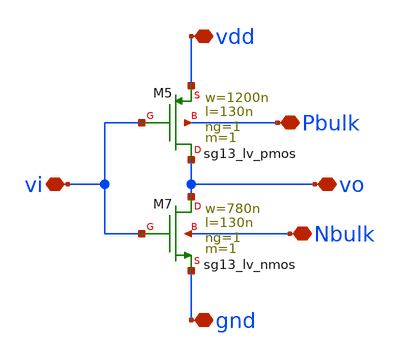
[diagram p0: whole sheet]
** sch_path: dependencies/SAH/SAH-main/schematic/xschem/inverter.sch
**.subckt inverter vi vo gnd vdd Pbulk Nbulk
*.iopin vi
*.iopin vo
*.iopin gnd
*.iopin vdd
*.iopin Pbulk
*.iopin Nbulk
XM5 vo vi vdd Pbulk sg13_lv_pmos w=1200n l=130n ng=1 m=1 mm_ok=1
XM7 vo vi gnd Nbulk sg13_lv_nmos w=780n l=130n ng=1 m=1 mm_ok=1
**.ends
.end
